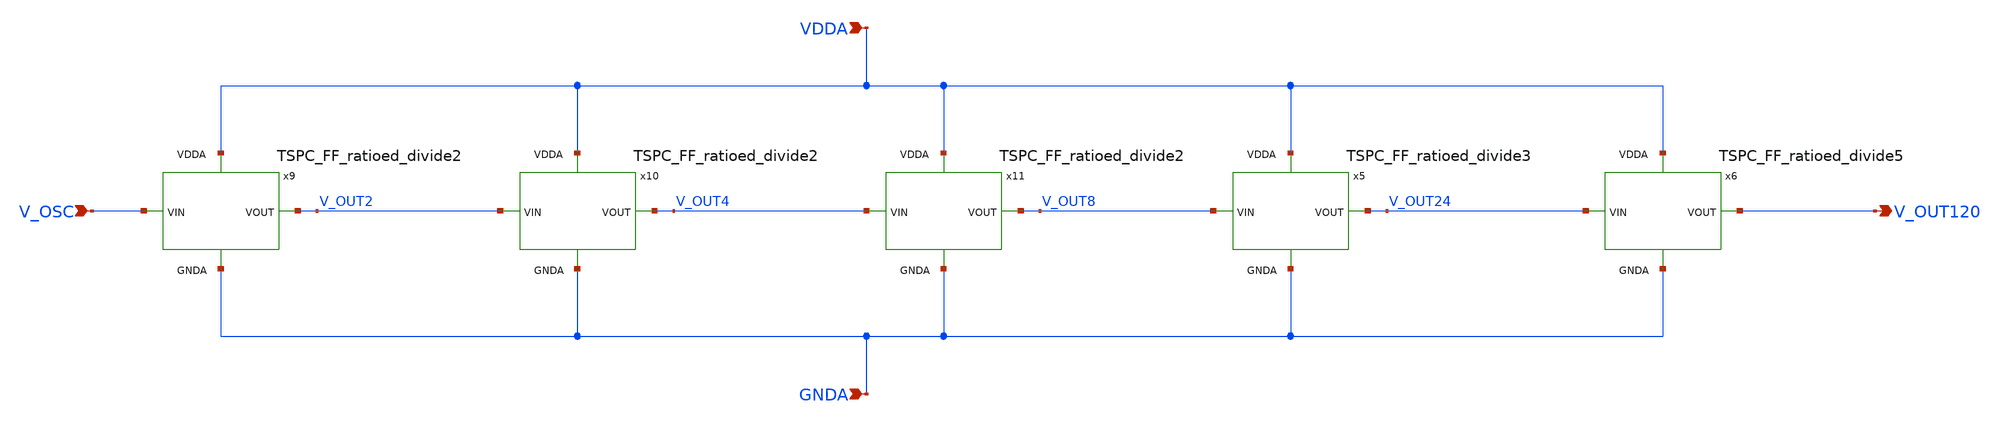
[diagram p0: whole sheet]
** sch_path: projects/pll/divider/xschem_ngspice/divide_by_120/divide_by_120.sch
**.subckt divide_by_120 V_OUT120 V_OSC GNDA VDDA
*.opin V_OUT120
*.ipin V_OSC
*.ipin GNDA
*.ipin VDDA
x5 V_OUT24 V_OUT8 VDDA GNDA TSPC_FF_ratioed_divide3
x6 V_OUT120 V_OUT24 VDDA GNDA TSPC_FF_ratioed_divide5
x9 V_OUT2 V_OSC VDDA GNDA TSPC_FF_ratioed_divide2
x10 V_OUT4 V_OUT2 VDDA GNDA TSPC_FF_ratioed_divide2
x11 V_OUT8 V_OUT4 VDDA GNDA TSPC_FF_ratioed_divide2
**.ends

* expanding   symbol:
*+  /foss/designs/my_design/projects/pll/divider/xschem_ngspice/TSPC_FF_ratioed_divide3.sym # of pins=4
** sym_path: projects/pll/divider/xschem_ngspice/TSPC_FF_ratioed_divide3.sym
** sch_path: projects/pll/divider/xschem_ngspice/TSPC_FF_ratioed_divide3.sch
.subckt TSPC_FF_ratioed_divide3 VOUT VIN VDDA GNDA
*.ipin VIN
*.opin VOUT
*.ipin VDDA
*.ipin GNDA
XM24 net7 VIN VDDA VDDA sky130_fd_pr__pfet_01v8 L=0.15 W=0.43 nf=1 ad='int((nf+1)/2) * W/nf * 0.29' as='int((nf+2)/2) * W/nf * 0.29'
+ pd='2*int((nf+1)/2) * (W/nf + 0.29)' ps='2*int((nf+2)/2) * (W/nf + 0.29)' nrd='0.29 / W' nrs='0.29 / W'
+ sa=0 sb=0 sd=0 mult=1 m=1
XM29 net7 net1 GNDA GNDA sky130_fd_pr__nfet_01v8 L=0.15 W=0.43 nf=1 ad='int((nf+1)/2) * W/nf * 0.29'
+ as='int((nf+2)/2) * W/nf * 0.29' pd='2*int((nf+1)/2) * (W/nf + 0.29)' ps='2*int((nf+2)/2) * (W/nf + 0.29)'
+ nrd='0.29 / W' nrs='0.29 / W' sa=0 sb=0 sd=0 mult=1 m=1
XM30 net1 net2 VDDA VDDA sky130_fd_pr__pfet_01v8 L=0.15 W=0.43 nf=1 ad='int((nf+1)/2) * W/nf * 0.29'
+ as='int((nf+2)/2) * W/nf * 0.29' pd='2*int((nf+1)/2) * (W/nf + 0.29)' ps='2*int((nf+2)/2) * (W/nf + 0.29)'
+ nrd='0.29 / W' nrs='0.29 / W' sa=0 sb=0 sd=0 mult=1 m=1
XM31 net1 VIN GNDA GNDA sky130_fd_pr__nfet_01v8 L=0.15 W=1.5 nf=1 ad='int((nf+1)/2) * W/nf * 0.29' as='int((nf+2)/2) * W/nf * 0.29'
+ pd='2*int((nf+1)/2) * (W/nf + 0.29)' ps='2*int((nf+2)/2) * (W/nf + 0.29)' nrd='0.29 / W' nrs='0.29 / W'
+ sa=0 sb=0 sd=0 mult=1 m=1
XM32 net2 VOUT VDDA VDDA sky130_fd_pr__pfet_01v8 L=0.15 W=0.43 nf=1 ad='int((nf+1)/2) * W/nf * 0.29'
+ as='int((nf+2)/2) * W/nf * 0.29' pd='2*int((nf+1)/2) * (W/nf + 0.29)' ps='2*int((nf+2)/2) * (W/nf + 0.29)'
+ nrd='0.29 / W' nrs='0.29 / W' sa=0 sb=0 sd=0 mult=1 m=1
XM33 net8 VOUT GNDA GNDA sky130_fd_pr__nfet_01v8 L=0.15 W=0.43 nf=1 ad='int((nf+1)/2) * W/nf * 0.29'
+ as='int((nf+2)/2) * W/nf * 0.29' pd='2*int((nf+1)/2) * (W/nf + 0.29)' ps='2*int((nf+2)/2) * (W/nf + 0.29)'
+ nrd='0.29 / W' nrs='0.29 / W' sa=0 sb=0 sd=0 mult=1 m=1
XM28 net2 VIN net8 GNDA sky130_fd_pr__nfet_01v8 L=0.15 W=0.43 nf=1 ad='int((nf+1)/2) * W/nf * 0.29' as='int((nf+2)/2) * W/nf * 0.29'
+ pd='2*int((nf+1)/2) * (W/nf + 0.29)' ps='2*int((nf+2)/2) * (W/nf + 0.29)' nrd='0.29 / W' nrs='0.29 / W'
+ sa=0 sb=0 sd=0 mult=1 m=1
XM34 net6 VIN VDDA VDDA sky130_fd_pr__pfet_01v8 L=0.15 W=0.43 nf=1 ad='int((nf+1)/2) * W/nf * 0.29' as='int((nf+2)/2) * W/nf * 0.29'
+ pd='2*int((nf+1)/2) * (W/nf + 0.29)' ps='2*int((nf+2)/2) * (W/nf + 0.29)' nrd='0.29 / W' nrs='0.29 / W'
+ sa=0 sb=0 sd=0 mult=1 m=1
XM39 net6 net4 GNDA GNDA sky130_fd_pr__nfet_01v8 L=0.15 W=0.43 nf=1 ad='int((nf+1)/2) * W/nf * 0.29'
+ as='int((nf+2)/2) * W/nf * 0.29' pd='2*int((nf+1)/2) * (W/nf + 0.29)' ps='2*int((nf+2)/2) * (W/nf + 0.29)'
+ nrd='0.29 / W' nrs='0.29 / W' sa=0 sb=0 sd=0 mult=1 m=1
XM40 net4 net5 VDDA VDDA sky130_fd_pr__pfet_01v8 L=0.15 W=0.43 nf=1 ad='int((nf+1)/2) * W/nf * 0.29'
+ as='int((nf+2)/2) * W/nf * 0.29' pd='2*int((nf+1)/2) * (W/nf + 0.29)' ps='2*int((nf+2)/2) * (W/nf + 0.29)'
+ nrd='0.29 / W' nrs='0.29 / W' sa=0 sb=0 sd=0 mult=1 m=1
XM41 net4 VIN GNDA GNDA sky130_fd_pr__nfet_01v8 L=0.15 W=1.5 nf=1 ad='int((nf+1)/2) * W/nf * 0.29' as='int((nf+2)/2) * W/nf * 0.29'
+ pd='2*int((nf+1)/2) * (W/nf + 0.29)' ps='2*int((nf+2)/2) * (W/nf + 0.29)' nrd='0.29 / W' nrs='0.29 / W'
+ sa=0 sb=0 sd=0 mult=1 m=1
XM42 net5 net6 VDDA VDDA sky130_fd_pr__pfet_01v8 L=0.15 W=0.43 nf=1 ad='int((nf+1)/2) * W/nf * 0.29'
+ as='int((nf+2)/2) * W/nf * 0.29' pd='2*int((nf+1)/2) * (W/nf + 0.29)' ps='2*int((nf+2)/2) * (W/nf + 0.29)'
+ nrd='0.29 / W' nrs='0.29 / W' sa=0 sb=0 sd=0 mult=1 m=1
XM43 net9 net7 net3 GNDA sky130_fd_pr__nfet_01v8 L=0.15 W=0.43 nf=1 ad='int((nf+1)/2) * W/nf * 0.29'
+ as='int((nf+2)/2) * W/nf * 0.29' pd='2*int((nf+1)/2) * (W/nf + 0.29)' ps='2*int((nf+2)/2) * (W/nf + 0.29)'
+ nrd='0.29 / W' nrs='0.29 / W' sa=0 sb=0 sd=0 mult=1 m=1
XM44 net5 VIN net9 GNDA sky130_fd_pr__nfet_01v8 L=0.15 W=0.43 nf=1 ad='int((nf+1)/2) * W/nf * 0.29' as='int((nf+2)/2) * W/nf * 0.29'
+ pd='2*int((nf+1)/2) * (W/nf + 0.29)' ps='2*int((nf+2)/2) * (W/nf + 0.29)' nrd='0.29 / W' nrs='0.29 / W'
+ sa=0 sb=0 sd=0 mult=1 m=1
XM4 VOUT net6 VDDA VDDA sky130_fd_pr__pfet_01v8 L=0.15 W=0.86 nf=2 ad='int((nf+1)/2) * W/nf * 0.29' as='int((nf+2)/2) * W/nf * 0.29'
+ pd='2*int((nf+1)/2) * (W/nf + 0.29)' ps='2*int((nf+2)/2) * (W/nf + 0.29)' nrd='0.29 / W' nrs='0.29 / W'
+ sa=0 sb=0 sd=0 mult=1 m=1
XM5 VOUT net6 GNDA GNDA sky130_fd_pr__nfet_01v8 L=0.15 W=0.43 nf=1 ad='int((nf+1)/2) * W/nf * 0.29' as='int((nf+2)/2) * W/nf * 0.29'
+ pd='2*int((nf+1)/2) * (W/nf + 0.29)' ps='2*int((nf+2)/2) * (W/nf + 0.29)' nrd='0.29 / W' nrs='0.29 / W'
+ sa=0 sb=0 sd=0 mult=1 m=1
XM6 net3 net6 GNDA GNDA sky130_fd_pr__nfet_01v8 L=0.15 W=0.43 nf=1 ad='int((nf+1)/2) * W/nf * 0.29' as='int((nf+2)/2) * W/nf * 0.29'
+ pd='2*int((nf+1)/2) * (W/nf + 0.29)' ps='2*int((nf+2)/2) * (W/nf + 0.29)' nrd='0.29 / W' nrs='0.29 / W'
+ sa=0 sb=0 sd=0 mult=1 m=1
XM7 net5 net7 VDDA VDDA sky130_fd_pr__pfet_01v8 L=0.15 W=0.43 nf=1 ad='int((nf+1)/2) * W/nf * 0.29' as='int((nf+2)/2) * W/nf * 0.29'
+ pd='2*int((nf+1)/2) * (W/nf + 0.29)' ps='2*int((nf+2)/2) * (W/nf + 0.29)' nrd='0.29 / W' nrs='0.29 / W'
+ sa=0 sb=0 sd=0 mult=1 m=1
.ends


* expanding   symbol:
*+  /foss/designs/my_design/projects/pll/divider/xschem_ngspice/TSPC_FF_ratioed_divide5.sym # of pins=4
** sym_path: projects/pll/divider/xschem_ngspice/TSPC_FF_ratioed_divide5.sym
** sch_path: projects/pll/divider/xschem_ngspice/TSPC_FF_ratioed_divide5.sch
.subckt TSPC_FF_ratioed_divide5 VOUT VIN VDDA GNDA
*.ipin VIN
*.opin VOUT
*.ipin VDDA
*.ipin GNDA
XM24 net11 VIN VDDA VDDA sky130_fd_pr__pfet_01v8 L=0.15 W=1 nf=1 ad='int((nf+1)/2) * W/nf * 0.29' as='int((nf+2)/2) * W/nf * 0.29'
+ pd='2*int((nf+1)/2) * (W/nf + 0.29)' ps='2*int((nf+2)/2) * (W/nf + 0.29)' nrd='0.29 / W' nrs='0.29 / W'
+ sa=0 sb=0 sd=0 mult=1 m=1
XM29 net11 net1 GNDA GNDA sky130_fd_pr__nfet_01v8 L=0.15 W=1 nf=1 ad='int((nf+1)/2) * W/nf * 0.29' as='int((nf+2)/2) * W/nf * 0.29'
+ pd='2*int((nf+1)/2) * (W/nf + 0.29)' ps='2*int((nf+2)/2) * (W/nf + 0.29)' nrd='0.29 / W' nrs='0.29 / W'
+ sa=0 sb=0 sd=0 mult=1 m=1
XM30 net1 net3 VDDA VDDA sky130_fd_pr__pfet_01v8 L=0.15 W=1 nf=1 ad='int((nf+1)/2) * W/nf * 0.29' as='int((nf+2)/2) * W/nf * 0.29'
+ pd='2*int((nf+1)/2) * (W/nf + 0.29)' ps='2*int((nf+2)/2) * (W/nf + 0.29)' nrd='0.29 / W' nrs='0.29 / W'
+ sa=0 sb=0 sd=0 mult=1 m=1
XM31 net1 VIN GNDA GNDA sky130_fd_pr__nfet_01v8 L=0.15 W=3 nf=3 ad='int((nf+1)/2) * W/nf * 0.29' as='int((nf+2)/2) * W/nf * 0.29'
+ pd='2*int((nf+1)/2) * (W/nf + 0.29)' ps='2*int((nf+2)/2) * (W/nf + 0.29)' nrd='0.29 / W' nrs='0.29 / W'
+ sa=0 sb=0 sd=0 mult=1 m=1
XM32 net3 net2 VDDA VDDA sky130_fd_pr__pfet_01v8 L=0.15 W=1 nf=1 ad='int((nf+1)/2) * W/nf * 0.29' as='int((nf+2)/2) * W/nf * 0.29'
+ pd='2*int((nf+1)/2) * (W/nf + 0.29)' ps='2*int((nf+2)/2) * (W/nf + 0.29)' nrd='0.29 / W' nrs='0.29 / W'
+ sa=0 sb=0 sd=0 mult=1 m=1
XM33 net12 net2 GNDA GNDA sky130_fd_pr__nfet_01v8 L=0.15 W=1 nf=1 ad='int((nf+1)/2) * W/nf * 0.29' as='int((nf+2)/2) * W/nf * 0.29'
+ pd='2*int((nf+1)/2) * (W/nf + 0.29)' ps='2*int((nf+2)/2) * (W/nf + 0.29)' nrd='0.29 / W' nrs='0.29 / W'
+ sa=0 sb=0 sd=0 mult=1 m=1
XM28 net3 VIN net12 GNDA sky130_fd_pr__nfet_01v8 L=0.15 W=1 nf=1 ad='int((nf+1)/2) * W/nf * 0.29' as='int((nf+2)/2) * W/nf * 0.29'
+ pd='2*int((nf+1)/2) * (W/nf + 0.29)' ps='2*int((nf+2)/2) * (W/nf + 0.29)' nrd='0.29 / W' nrs='0.29 / W'
+ sa=0 sb=0 sd=0 mult=1 m=1
XM34 net7 VIN VDDA VDDA sky130_fd_pr__pfet_01v8 L=0.15 W=1 nf=1 ad='int((nf+1)/2) * W/nf * 0.29' as='int((nf+2)/2) * W/nf * 0.29'
+ pd='2*int((nf+1)/2) * (W/nf + 0.29)' ps='2*int((nf+2)/2) * (W/nf + 0.29)' nrd='0.29 / W' nrs='0.29 / W'
+ sa=0 sb=0 sd=0 mult=1 m=1
XM39 net7 net5 GNDA GNDA sky130_fd_pr__nfet_01v8 L=0.15 W=1 nf=1 ad='int((nf+1)/2) * W/nf * 0.29' as='int((nf+2)/2) * W/nf * 0.29'
+ pd='2*int((nf+1)/2) * (W/nf + 0.29)' ps='2*int((nf+2)/2) * (W/nf + 0.29)' nrd='0.29 / W' nrs='0.29 / W'
+ sa=0 sb=0 sd=0 mult=1 m=1
XM40 net5 net6 VDDA VDDA sky130_fd_pr__pfet_01v8 L=0.15 W=1 nf=1 ad='int((nf+1)/2) * W/nf * 0.29' as='int((nf+2)/2) * W/nf * 0.29'
+ pd='2*int((nf+1)/2) * (W/nf + 0.29)' ps='2*int((nf+2)/2) * (W/nf + 0.29)' nrd='0.29 / W' nrs='0.29 / W'
+ sa=0 sb=0 sd=0 mult=1 m=1
XM41 net5 VIN GNDA GNDA sky130_fd_pr__nfet_01v8 L=0.15 W=3 nf=3 ad='int((nf+1)/2) * W/nf * 0.29' as='int((nf+2)/2) * W/nf * 0.29'
+ pd='2*int((nf+1)/2) * (W/nf + 0.29)' ps='2*int((nf+2)/2) * (W/nf + 0.29)' nrd='0.29 / W' nrs='0.29 / W'
+ sa=0 sb=0 sd=0 mult=1 m=1
XM42 net6 VOUT net8 VDDA sky130_fd_pr__pfet_01v8 L=0.15 W=1 nf=1 ad='int((nf+1)/2) * W/nf * 0.29' as='int((nf+2)/2) * W/nf * 0.29'
+ pd='2*int((nf+1)/2) * (W/nf + 0.29)' ps='2*int((nf+2)/2) * (W/nf + 0.29)' nrd='0.29 / W' nrs='0.29 / W'
+ sa=0 sb=0 sd=0 mult=1 m=1
XM43 net13 net7 net4 GNDA sky130_fd_pr__nfet_01v8 L=0.15 W=1 nf=1 ad='int((nf+1)/2) * W/nf * 0.29' as='int((nf+2)/2) * W/nf * 0.29'
+ pd='2*int((nf+1)/2) * (W/nf + 0.29)' ps='2*int((nf+2)/2) * (W/nf + 0.29)' nrd='0.29 / W' nrs='0.29 / W'
+ sa=0 sb=0 sd=0 mult=1 m=1
XM44 net6 VIN net13 GNDA sky130_fd_pr__nfet_01v8 L=0.15 W=1 nf=1 ad='int((nf+1)/2) * W/nf * 0.29' as='int((nf+2)/2) * W/nf * 0.29'
+ pd='2*int((nf+1)/2) * (W/nf + 0.29)' ps='2*int((nf+2)/2) * (W/nf + 0.29)' nrd='0.29 / W' nrs='0.29 / W'
+ sa=0 sb=0 sd=0 mult=1 m=1
XM4 net2 net7 VDDA VDDA sky130_fd_pr__pfet_01v8 L=0.15 W=2 nf=2 ad='int((nf+1)/2) * W/nf * 0.29' as='int((nf+2)/2) * W/nf * 0.29'
+ pd='2*int((nf+1)/2) * (W/nf + 0.29)' ps='2*int((nf+2)/2) * (W/nf + 0.29)' nrd='0.29 / W' nrs='0.29 / W'
+ sa=0 sb=0 sd=0 mult=1 m=1
XM5 net2 net7 GNDA GNDA sky130_fd_pr__nfet_01v8 L=0.15 W=1 nf=1 ad='int((nf+1)/2) * W/nf * 0.29' as='int((nf+2)/2) * W/nf * 0.29'
+ pd='2*int((nf+1)/2) * (W/nf + 0.29)' ps='2*int((nf+2)/2) * (W/nf + 0.29)' nrd='0.29 / W' nrs='0.29 / W'
+ sa=0 sb=0 sd=0 mult=1 m=1
XM6 net4 VOUT GNDA GNDA sky130_fd_pr__nfet_01v8 L=0.15 W=1 nf=1 ad='int((nf+1)/2) * W/nf * 0.29' as='int((nf+2)/2) * W/nf * 0.29'
+ pd='2*int((nf+1)/2) * (W/nf + 0.29)' ps='2*int((nf+2)/2) * (W/nf + 0.29)' nrd='0.29 / W' nrs='0.29 / W'
+ sa=0 sb=0 sd=0 mult=1 m=1
XM7 net6 net7 VDDA VDDA sky130_fd_pr__pfet_01v8 L=0.15 W=1 nf=1 ad='int((nf+1)/2) * W/nf * 0.29' as='int((nf+2)/2) * W/nf * 0.29'
+ pd='2*int((nf+1)/2) * (W/nf + 0.29)' ps='2*int((nf+2)/2) * (W/nf + 0.29)' nrd='0.29 / W' nrs='0.29 / W'
+ sa=0 sb=0 sd=0 mult=1 m=1
XM1 net8 net11 VDDA VDDA sky130_fd_pr__pfet_01v8 L=0.15 W=1 nf=1 ad='int((nf+1)/2) * W/nf * 0.29' as='int((nf+2)/2) * W/nf * 0.29'
+ pd='2*int((nf+1)/2) * (W/nf + 0.29)' ps='2*int((nf+2)/2) * (W/nf + 0.29)' nrd='0.29 / W' nrs='0.29 / W'
+ sa=0 sb=0 sd=0 mult=1 m=1
XM2 net4 net11 GNDA GNDA sky130_fd_pr__nfet_01v8 L=0.15 W=1 nf=1 ad='int((nf+1)/2) * W/nf * 0.29' as='int((nf+2)/2) * W/nf * 0.29'
+ pd='2*int((nf+1)/2) * (W/nf + 0.29)' ps='2*int((nf+2)/2) * (W/nf + 0.29)' nrd='0.29 / W' nrs='0.29 / W'
+ sa=0 sb=0 sd=0 mult=1 m=1
XM3 VOUT net7 VDDA VDDA sky130_fd_pr__pfet_01v8 L=0.15 W=1 nf=1 ad='int((nf+1)/2) * W/nf * 0.29' as='int((nf+2)/2) * W/nf * 0.29'
+ pd='2*int((nf+1)/2) * (W/nf + 0.29)' ps='2*int((nf+2)/2) * (W/nf + 0.29)' nrd='0.29 / W' nrs='0.29 / W'
+ sa=0 sb=0 sd=0 mult=1 m=1
XM8 VOUT net9 GNDA GNDA sky130_fd_pr__nfet_01v8 L=0.15 W=1 nf=1 ad='int((nf+1)/2) * W/nf * 0.29' as='int((nf+2)/2) * W/nf * 0.29'
+ pd='2*int((nf+1)/2) * (W/nf + 0.29)' ps='2*int((nf+2)/2) * (W/nf + 0.29)' nrd='0.29 / W' nrs='0.29 / W'
+ sa=0 sb=0 sd=0 mult=1 m=1
XM9 net9 net10 VDDA VDDA sky130_fd_pr__pfet_01v8 L=0.15 W=1 nf=1 ad='int((nf+1)/2) * W/nf * 0.29' as='int((nf+2)/2) * W/nf * 0.29'
+ pd='2*int((nf+1)/2) * (W/nf + 0.29)' ps='2*int((nf+2)/2) * (W/nf + 0.29)' nrd='0.29 / W' nrs='0.29 / W'
+ sa=0 sb=0 sd=0 mult=1 m=1
XM10 net9 net7 GNDA GNDA sky130_fd_pr__nfet_01v8 L=0.15 W=3 nf=3 ad='int((nf+1)/2) * W/nf * 0.29' as='int((nf+2)/2) * W/nf * 0.29'
+ pd='2*int((nf+1)/2) * (W/nf + 0.29)' ps='2*int((nf+2)/2) * (W/nf + 0.29)' nrd='0.29 / W' nrs='0.29 / W'
+ sa=0 sb=0 sd=0 mult=1 m=1
XM11 net10 VOUT VDDA VDDA sky130_fd_pr__pfet_01v8 L=0.15 W=1 nf=1 ad='int((nf+1)/2) * W/nf * 0.29' as='int((nf+2)/2) * W/nf * 0.29'
+ pd='2*int((nf+1)/2) * (W/nf + 0.29)' ps='2*int((nf+2)/2) * (W/nf + 0.29)' nrd='0.29 / W' nrs='0.29 / W'
+ sa=0 sb=0 sd=0 mult=1 m=1
XM12 net14 VOUT GNDA GNDA sky130_fd_pr__nfet_01v8 L=0.15 W=1 nf=1 ad='int((nf+1)/2) * W/nf * 0.29' as='int((nf+2)/2) * W/nf * 0.29'
+ pd='2*int((nf+1)/2) * (W/nf + 0.29)' ps='2*int((nf+2)/2) * (W/nf + 0.29)' nrd='0.29 / W' nrs='0.29 / W'
+ sa=0 sb=0 sd=0 mult=1 m=1
XM13 net10 net7 net14 GNDA sky130_fd_pr__nfet_01v8 L=0.15 W=1 nf=1 ad='int((nf+1)/2) * W/nf * 0.29' as='int((nf+2)/2) * W/nf * 0.29'
+ pd='2*int((nf+1)/2) * (W/nf + 0.29)' ps='2*int((nf+2)/2) * (W/nf + 0.29)' nrd='0.29 / W' nrs='0.29 / W'
+ sa=0 sb=0 sd=0 mult=1 m=1
.ends


* expanding   symbol:
*+  /foss/designs/my_design/projects/pll/divider/xschem_ngspice/TSPC_FF_ratioed_divide2.sym # of pins=4
** sym_path: projects/pll/divider/xschem_ngspice/TSPC_FF_ratioed_divide2.sym
** sch_path: projects/pll/divider/xschem_ngspice/TSPC_FF_ratioed_divide2.sch
.subckt TSPC_FF_ratioed_divide2 VOUT VIN VDDA GNDA
*.ipin VIN
*.opin VOUT
*.ipin VDDA
*.ipin GNDA
XM24 VOUT VIN VDDA VDDA sky130_fd_pr__pfet_01v8 L=0.15 W=1 nf=1 ad='int((nf+1)/2) * W/nf * 0.29' as='int((nf+2)/2) * W/nf * 0.29'
+ pd='2*int((nf+1)/2) * (W/nf + 0.29)' ps='2*int((nf+2)/2) * (W/nf + 0.29)' nrd='0.29 / W' nrs='0.29 / W'
+ sa=0 sb=0 sd=0 mult=1 m=1
XM29 VOUT net1 GNDA GNDA sky130_fd_pr__nfet_01v8 L=0.15 W=1 nf=1 ad='int((nf+1)/2) * W/nf * 0.29' as='int((nf+2)/2) * W/nf * 0.29'
+ pd='2*int((nf+1)/2) * (W/nf + 0.29)' ps='2*int((nf+2)/2) * (W/nf + 0.29)' nrd='0.29 / W' nrs='0.29 / W'
+ sa=0 sb=0 sd=0 mult=1 m=1
XM30 net1 net2 VDDA VDDA sky130_fd_pr__pfet_01v8 L=0.15 W=1 nf=1 ad='int((nf+1)/2) * W/nf * 0.29' as='int((nf+2)/2) * W/nf * 0.29'
+ pd='2*int((nf+1)/2) * (W/nf + 0.29)' ps='2*int((nf+2)/2) * (W/nf + 0.29)' nrd='0.29 / W' nrs='0.29 / W'
+ sa=0 sb=0 sd=0 mult=1 m=1
XM31 net1 VIN GNDA GNDA sky130_fd_pr__nfet_01v8 L=0.15 W=3 nf=3 ad='int((nf+1)/2) * W/nf * 0.29' as='int((nf+2)/2) * W/nf * 0.29'
+ pd='2*int((nf+1)/2) * (W/nf + 0.29)' ps='2*int((nf+2)/2) * (W/nf + 0.29)' nrd='0.29 / W' nrs='0.29 / W'
+ sa=0 sb=0 sd=0 mult=1 m=1
XM32 net2 VOUT VDDA VDDA sky130_fd_pr__pfet_01v8 L=0.15 W=1 nf=1 ad='int((nf+1)/2) * W/nf * 0.29' as='int((nf+2)/2) * W/nf * 0.29'
+ pd='2*int((nf+1)/2) * (W/nf + 0.29)' ps='2*int((nf+2)/2) * (W/nf + 0.29)' nrd='0.29 / W' nrs='0.29 / W'
+ sa=0 sb=0 sd=0 mult=1 m=1
XM33 net3 VOUT GNDA GNDA sky130_fd_pr__nfet_01v8 L=0.15 W=1 nf=1 ad='int((nf+1)/2) * W/nf * 0.29' as='int((nf+2)/2) * W/nf * 0.29'
+ pd='2*int((nf+1)/2) * (W/nf + 0.29)' ps='2*int((nf+2)/2) * (W/nf + 0.29)' nrd='0.29 / W' nrs='0.29 / W'
+ sa=0 sb=0 sd=0 mult=1 m=1
XM28 net2 VIN net3 GNDA sky130_fd_pr__nfet_01v8 L=0.15 W=1 nf=1 ad='int((nf+1)/2) * W/nf * 0.29' as='int((nf+2)/2) * W/nf * 0.29'
+ pd='2*int((nf+1)/2) * (W/nf + 0.29)' ps='2*int((nf+2)/2) * (W/nf + 0.29)' nrd='0.29 / W' nrs='0.29 / W'
+ sa=0 sb=0 sd=0 mult=1 m=1
.ends

.end
